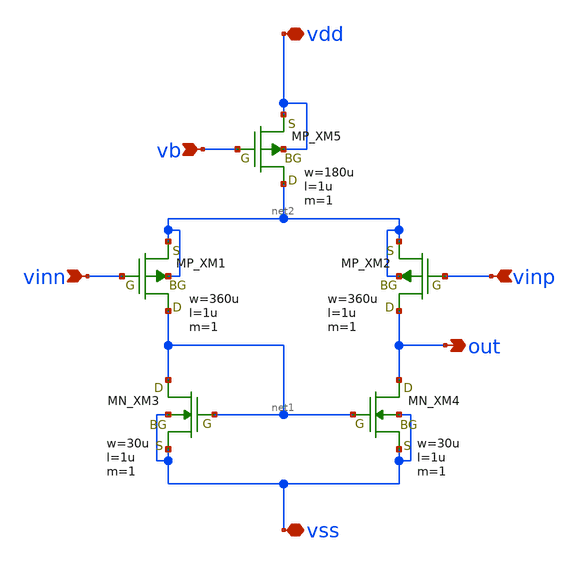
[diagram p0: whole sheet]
** sch_path: schematic/20250924_OSS_Workshop/ishikai/opamp/sample/diff.sch
**.subckt diff vinn vinp vb out vdd vss
*.ipin vinn
*.ipin vinp
*.ipin vb
*.opin out
*.iopin vdd
*.iopin vss
XM5 net2 vb vdd vdd PMOS w=180u l=1u as=0 ad=0 ps=0 pd=0 nrd=0 nrs=0 m=1
XM1 net1 vinn net2 net2 PMOS w=360u l=1u as=0 ad=0 ps=0 pd=0 nrd=0 nrs=0 m=1
XM2 out vinp net2 net2 PMOS w=360u l=1u as=0 ad=0 ps=0 pd=0 nrd=0 nrs=0 m=1
XM3 net1 net1 vss vss NMOS w=30u l=1u as=0 ad=0 ps=0 pd=0 nrd=0 nrs=0 m=1
XM4 out net1 vss vss NMOS w=30u l=1u as=0 ad=0 ps=0 pd=0 nrd=0 nrs=0 m=1
**.ends
.end
